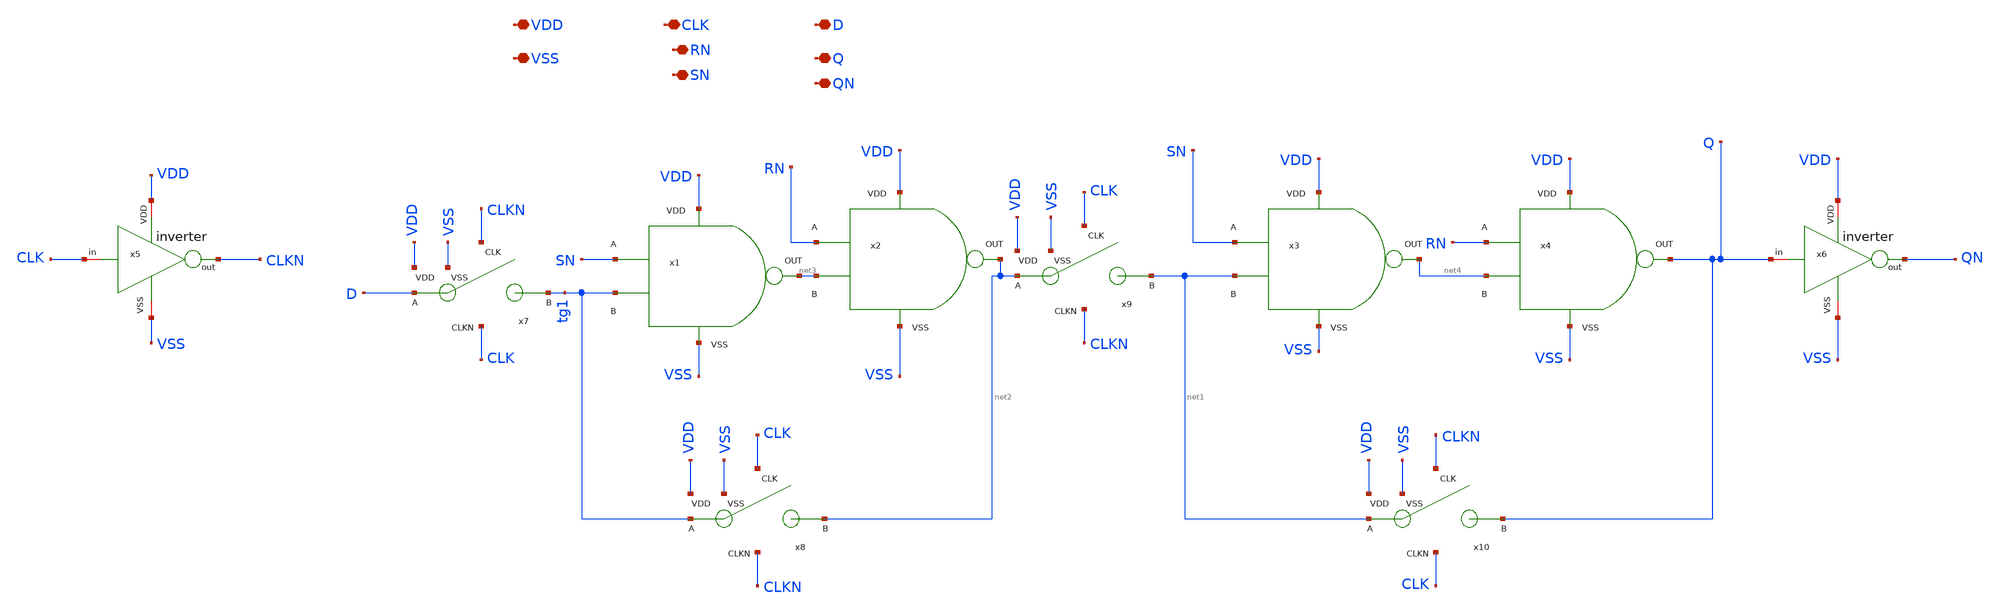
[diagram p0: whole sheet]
** sch_path: designs/sar_adc/digital/flip_flop_set/xschem/flip_flop_set.sch
**.subckt flip_flop_set VDD VSS CLK D RN Q QN SN
*.iopin VDD
*.iopin VSS
*.iopin CLK
*.iopin D
*.iopin RN
*.iopin Q
*.iopin QN
*.iopin SN
x1 VDD VSS SN tg1 net3 NAND
x2 VDD VSS RN net3 net2 NAND
x3 VDD VSS SN net1 net4 NAND
x4 VDD VSS RN net4 Q NAND
x5 VDD CLK CLKN VSS inverter
x6 VDD Q QN VSS inverter
x7 CLKN D VDD tg1 CLK VSS TG
x8 CLK tg1 VDD net2 CLKN VSS TG
x9 CLK net2 VDD net1 CLKN VSS TG
x10 CLKN net1 VDD Q CLK VSS TG
**.ends

* expanding   symbol:  designs/sar_adc/digital/NAND/xschem/NAND.sym # of pins=5
** sym_path: designs/sar_adc/digital/NAND/xschem/NAND.sym
** sch_path: designs/sar_adc/digital/NAND/xschem/NAND.sch
.subckt NAND VDD VSS A B out
*.iopin VDD
*.iopin A
*.iopin B
*.iopin out
*.iopin VSS
xINVA VDD net1 net2 VSS inverter
xINVB[2] VDD net2 out VSS inverter
xINVB[1] VDD net2 out VSS inverter
xINVB[0] VDD net2 out VSS inverter
XM2 net1 A VDD VDD pfet_03v3 L=0.28u W=0.5u nf=1 ad='int((nf+1)/2) * W/nf * 0.18u' as='int((nf+2)/2) * W/nf * 0.18u'
+ pd='2*int((nf+1)/2) * (W/nf + 0.18u)' ps='2*int((nf+2)/2) * (W/nf + 0.18u)' nrd='0.18u / W' nrs='0.18u / W'
+ sa=0 sb=0 sd=0 m=2
XM1 net1 A net3 VSS nfet_03v3 L=0.28u W=0.5u nf=1 ad='int((nf+1)/2) * W/nf * 0.18u' as='int((nf+2)/2) * W/nf * 0.18u'
+ pd='2*int((nf+1)/2) * (W/nf + 0.18u)' ps='2*int((nf+2)/2) * (W/nf + 0.18u)' nrd='0.18u / W' nrs='0.18u / W'
+ sa=0 sb=0 sd=0 m=1
XM3 net1 B VDD VDD pfet_03v3 L=0.28u W=0.5u nf=1 ad='int((nf+1)/2) * W/nf * 0.18u' as='int((nf+2)/2) * W/nf * 0.18u'
+ pd='2*int((nf+1)/2) * (W/nf + 0.18u)' ps='2*int((nf+2)/2) * (W/nf + 0.18u)' nrd='0.18u / W' nrs='0.18u / W'
+ sa=0 sb=0 sd=0 m=2
XM4 net3 B VSS VSS nfet_03v3 L=0.28u W=0.5u nf=1 ad='int((nf+1)/2) * W/nf * 0.18u' as='int((nf+2)/2) * W/nf * 0.18u'
+ pd='2*int((nf+1)/2) * (W/nf + 0.18u)' ps='2*int((nf+2)/2) * (W/nf + 0.18u)' nrd='0.18u / W' nrs='0.18u / W'
+ sa=0 sb=0 sd=0 m=1
.ends


* expanding   symbol:  designs/sar_adc/digital/buffer_inv_x1/xschem/inverter.sym # of pins=6
** sym_path: designs/sar_adc/digital/buffer_inv_x1/xschem/inverter.sym
** sch_path: designs/sar_adc/digital/buffer_inv_x1/xschem/inverter.sch
.subckt inverter VDD in out VSS
*.opin out
*.iopin in
*.iopin VDD
*.iopin VSS
XM1 out in VSS VSS nfet_03v3 L=0.56u W=0.25u nf=1 ad='int((nf+1)/2) * W/nf * 0.18u' as='int((nf+2)/2) * W/nf * 0.18u'
+ pd='2*int((nf+1)/2) * (W/nf + 0.18u)' ps='2*int((nf+2)/2) * (W/nf + 0.18u)' nrd='0.18u / W' nrs='0.18u / W'
+ sa=0 sb=0 sd=0 m=2
XM2 out in VDD VDD pfet_03v3 L=0.56u W=0.25u nf=1 ad='int((nf+1)/2) * W/nf * 0.18u' as='int((nf+2)/2) * W/nf * 0.18u'
+ pd='2*int((nf+1)/2) * (W/nf + 0.18u)' ps='2*int((nf+2)/2) * (W/nf + 0.18u)' nrd='0.18u / W' nrs='0.18u / W'
+ sa=0 sb=0 sd=0 m=4
.ends


* expanding   symbol:  designs/sar_adc/digital/TG/xschem/TG.sym # of pins=6
** sym_path: designs/sar_adc/digital/TG/xschem/TG.sym
** sch_path: designs/sar_adc/digital/TG/xschem/TG.sch
.subckt TG CLK A VDD B CLKN VSS
*.iopin VDD
*.iopin VSS
*.ipin CLK
*.ipin CLKN
*.iopin A
*.iopin B
XM1 A CLK B VSS nfet_03v3 L=0.28u W=0.22u nf=1 ad='int((nf+1)/2) * W/nf * 0.18u' as='int((nf+2)/2) * W/nf * 0.18u'
+ pd='2*int((nf+1)/2) * (W/nf + 0.18u)' ps='2*int((nf+2)/2) * (W/nf + 0.18u)' nrd='0.18u / W' nrs='0.18u / W'
+ sa=0 sb=0 sd=0 m=1
XM2 A CLKN B VDD pfet_03v3 L=0.28u W=0.22u nf=1 ad='int((nf+1)/2) * W/nf * 0.18u' as='int((nf+2)/2) * W/nf * 0.18u'
+ pd='2*int((nf+1)/2) * (W/nf + 0.18u)' ps='2*int((nf+2)/2) * (W/nf + 0.18u)' nrd='0.18u / W' nrs='0.18u / W'
+ sa=0 sb=0 sd=0 m=1
.ends

.end
